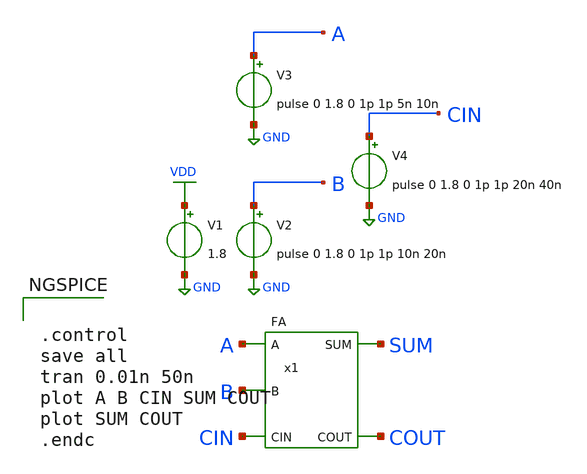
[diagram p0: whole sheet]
** sch_path: lib/xschem/test_FA.sch
**.subckt test_FA
V2 B GND pulse 0 1.8 0 1p 1p 10n 20n
V1 VDD GND 1.8
V3 A GND pulse 0 1.8 0 1p 1p 5n 10n
x1 SUM COUT A B CIN VDD GND FA
V4 CIN GND pulse 0 1.8 0 1p 1p 20n 40n
**** begin user architecture code

.lib $::SKYWATER_MODELS/sky130.lib.spice tt


**** end user architecture code
**.ends

* expanding   symbol:  FA.sym # of pins=5
** sym_path: lib/xschem/FA.sym
** sch_path: lib/xschem/FA.sch
.subckt FA SUM COUT A B CIN VCCPIN VSSPIN
*.opin COUT
*.ipin A
*.ipin B
*.ipin CIN
*.opin SUM
x1 net2 CIN net1 VCCPIN VSSPIN AND2X1
x2 net1 A B VCCPIN VSSPIN XOR2X1
x3 SUM net1 CIN VCCPIN VSSPIN XOR2X1
x4 net3 B A VCCPIN VSSPIN AND2X1
x5 COUT net2 net3 VCCPIN VSSPIN OR2X1
.ends


* expanding   symbol:  AND2X1.sym # of pins=3
** sym_path: lib/xschem/AND2X1.sym
** sch_path: lib/xschem/AND2X1.sch
.subckt AND2X1 Y A B VCCPIN VSSPIN
*.ipin A
*.ipin B
*.opin Y
x1 net1 A B NAND2X1
x2 Y net1 INVX1
.ends


* expanding   symbol:  XOR2X1.sym # of pins=3
** sym_path: lib/xschem/XOR2X1.sym
** sch_path: lib/xschem/XOR2X1.sch
.subckt XOR2X1 Y A B VCCPIN VSSPIN
*.ipin A
*.opin Y
*.ipin B
XM1 net6 A VSSPIN GND sky130_fd_pr__nfet_01v8 L=0.15 W=3 nf=1 ad='int((nf+1)/2) * W/nf * 0.29' as='int((nf+2)/2) * W/nf * 0.29'
+ pd='2*int((nf+1)/2) * (W/nf + 0.29)' ps='2*int((nf+2)/2) * (W/nf + 0.29)' nrd='0.29 / W' nrs='0.29 / W'
+ sa=0 sb=0 sd=0 mult=1 m=1
XM2 net6 A VCCPIN VDD sky130_fd_pr__pfet_01v8 L=0.15 W=2 nf=1 ad='int((nf+1)/2) * W/nf * 0.29' as='int((nf+2)/2) * W/nf * 0.29'
+ pd='2*int((nf+1)/2) * (W/nf + 0.29)' ps='2*int((nf+2)/2) * (W/nf + 0.29)' nrd='0.29 / W' nrs='0.29 / W'
+ sa=0 sb=0 sd=0 mult=1 m=1
XM3 net3 B VSSPIN GND sky130_fd_pr__nfet_01v8 L=0.15 W=3 nf=1 ad='int((nf+1)/2) * W/nf * 0.29' as='int((nf+2)/2) * W/nf * 0.29'
+ pd='2*int((nf+1)/2) * (W/nf + 0.29)' ps='2*int((nf+2)/2) * (W/nf + 0.29)' nrd='0.29 / W' nrs='0.29 / W'
+ sa=0 sb=0 sd=0 mult=1 m=1
XM4 net3 B VCCPIN VDD sky130_fd_pr__pfet_01v8 L=0.15 W=2 nf=1 ad='int((nf+1)/2) * W/nf * 0.29' as='int((nf+2)/2) * W/nf * 0.29'
+ pd='2*int((nf+1)/2) * (W/nf + 0.29)' ps='2*int((nf+2)/2) * (W/nf + 0.29)' nrd='0.29 / W' nrs='0.29 / W'
+ sa=0 sb=0 sd=0 mult=1 m=1
XM5 net4 net3 VCCPIN VDD sky130_fd_pr__pfet_01v8 L=0.15 W=2 nf=1 ad='int((nf+1)/2) * W/nf * 0.29' as='int((nf+2)/2) * W/nf * 0.29'
+ pd='2*int((nf+1)/2) * (W/nf + 0.29)' ps='2*int((nf+2)/2) * (W/nf + 0.29)' nrd='0.29 / W' nrs='0.29 / W'
+ sa=0 sb=0 sd=0 mult=1 m=1
XM6 Y A net4 VDD sky130_fd_pr__pfet_01v8 L=0.15 W=2 nf=1 ad='int((nf+1)/2) * W/nf * 0.29' as='int((nf+2)/2) * W/nf * 0.29'
+ pd='2*int((nf+1)/2) * (W/nf + 0.29)' ps='2*int((nf+2)/2) * (W/nf + 0.29)' nrd='0.29 / W' nrs='0.29 / W'
+ sa=0 sb=0 sd=0 mult=1 m=1
XM7 net2 B VCCPIN VDD sky130_fd_pr__pfet_01v8 L=0.15 W=2 nf=1 ad='int((nf+1)/2) * W/nf * 0.29' as='int((nf+2)/2) * W/nf * 0.29'
+ pd='2*int((nf+1)/2) * (W/nf + 0.29)' ps='2*int((nf+2)/2) * (W/nf + 0.29)' nrd='0.29 / W' nrs='0.29 / W'
+ sa=0 sb=0 sd=0 mult=1 m=1
XM8 Y net6 net2 VDD sky130_fd_pr__pfet_01v8 L=0.15 W=2 nf=1 ad='int((nf+1)/2) * W/nf * 0.29' as='int((nf+2)/2) * W/nf * 0.29'
+ pd='2*int((nf+1)/2) * (W/nf + 0.29)' ps='2*int((nf+2)/2) * (W/nf + 0.29)' nrd='0.29 / W' nrs='0.29 / W'
+ sa=0 sb=0 sd=0 mult=1 m=1
XM9 Y net6 net1 GND sky130_fd_pr__nfet_01v8 L=0.15 W=3 nf=1 ad='int((nf+1)/2) * W/nf * 0.29' as='int((nf+2)/2) * W/nf * 0.29'
+ pd='2*int((nf+1)/2) * (W/nf + 0.29)' ps='2*int((nf+2)/2) * (W/nf + 0.29)' nrd='0.29 / W' nrs='0.29 / W'
+ sa=0 sb=0 sd=0 mult=1 m=1
XM10 net1 net3 VSSPIN GND sky130_fd_pr__nfet_01v8 L=0.15 W=3 nf=1 ad='int((nf+1)/2) * W/nf * 0.29' as='int((nf+2)/2) * W/nf * 0.29'
+ pd='2*int((nf+1)/2) * (W/nf + 0.29)' ps='2*int((nf+2)/2) * (W/nf + 0.29)' nrd='0.29 / W' nrs='0.29 / W'
+ sa=0 sb=0 sd=0 mult=1 m=1
XM11 Y A net5 GND sky130_fd_pr__nfet_01v8 L=0.15 W=3 nf=1 ad='int((nf+1)/2) * W/nf * 0.29' as='int((nf+2)/2) * W/nf * 0.29'
+ pd='2*int((nf+1)/2) * (W/nf + 0.29)' ps='2*int((nf+2)/2) * (W/nf + 0.29)' nrd='0.29 / W' nrs='0.29 / W'
+ sa=0 sb=0 sd=0 mult=1 m=1
XM12 net5 B VSSPIN GND sky130_fd_pr__nfet_01v8 L=0.15 W=3 nf=1 ad='int((nf+1)/2) * W/nf * 0.29' as='int((nf+2)/2) * W/nf * 0.29'
+ pd='2*int((nf+1)/2) * (W/nf + 0.29)' ps='2*int((nf+2)/2) * (W/nf + 0.29)' nrd='0.29 / W' nrs='0.29 / W'
+ sa=0 sb=0 sd=0 mult=1 m=1
XM13 net4 net3 VCCPIN VDD sky130_fd_pr__pfet_01v8 L=0.15 W=2 nf=1 ad='int((nf+1)/2) * W/nf * 0.29' as='int((nf+2)/2) * W/nf * 0.29'
+ pd='2*int((nf+1)/2) * (W/nf + 0.29)' ps='2*int((nf+2)/2) * (W/nf + 0.29)' nrd='0.29 / W' nrs='0.29 / W'
+ sa=0 sb=0 sd=0 mult=1 m=1
XM14 Y A net4 VDD sky130_fd_pr__pfet_01v8 L=0.15 W=2 nf=1 ad='int((nf+1)/2) * W/nf * 0.29' as='int((nf+2)/2) * W/nf * 0.29'
+ pd='2*int((nf+1)/2) * (W/nf + 0.29)' ps='2*int((nf+2)/2) * (W/nf + 0.29)' nrd='0.29 / W' nrs='0.29 / W'
+ sa=0 sb=0 sd=0 mult=1 m=1
XM15 net2 B VCCPIN VDD sky130_fd_pr__pfet_01v8 L=0.15 W=2 nf=1 ad='int((nf+1)/2) * W/nf * 0.29' as='int((nf+2)/2) * W/nf * 0.29'
+ pd='2*int((nf+1)/2) * (W/nf + 0.29)' ps='2*int((nf+2)/2) * (W/nf + 0.29)' nrd='0.29 / W' nrs='0.29 / W'
+ sa=0 sb=0 sd=0 mult=1 m=1
XM16 Y net6 net2 VDD sky130_fd_pr__pfet_01v8 L=0.15 W=2 nf=1 ad='int((nf+1)/2) * W/nf * 0.29' as='int((nf+2)/2) * W/nf * 0.29'
+ pd='2*int((nf+1)/2) * (W/nf + 0.29)' ps='2*int((nf+2)/2) * (W/nf + 0.29)' nrd='0.29 / W' nrs='0.29 / W'
+ sa=0 sb=0 sd=0 mult=1 m=1
XM17 net3 B VCCPIN VDD sky130_fd_pr__pfet_01v8 L=0.15 W=2 nf=1 ad='int((nf+1)/2) * W/nf * 0.29' as='int((nf+2)/2) * W/nf * 0.29'
+ pd='2*int((nf+1)/2) * (W/nf + 0.29)' ps='2*int((nf+2)/2) * (W/nf + 0.29)' nrd='0.29 / W' nrs='0.29 / W'
+ sa=0 sb=0 sd=0 mult=1 m=1
XM18 net6 A VCCPIN VDD sky130_fd_pr__pfet_01v8 L=0.15 W=2 nf=1 ad='int((nf+1)/2) * W/nf * 0.29' as='int((nf+2)/2) * W/nf * 0.29'
+ pd='2*int((nf+1)/2) * (W/nf + 0.29)' ps='2*int((nf+2)/2) * (W/nf + 0.29)' nrd='0.29 / W' nrs='0.29 / W'
+ sa=0 sb=0 sd=0 mult=1 m=1
.ends


* expanding   symbol:  OR2X1.sym # of pins=3
** sym_path: lib/xschem/OR2X1.sym
** sch_path: lib/xschem/OR2X1.sch
.subckt OR2X1 Y A B VCCPIN VSSPIN
*.ipin A
*.ipin B
*.opin Y
x1 net1 A B NOR2X1
x2 Y net1 INVX1
.ends


* expanding   symbol:  NAND2X1.sym # of pins=3
** sym_path: lib/xschem/NAND2X1.sym
** sch_path: lib/xschem/NAND2X1.sch
.subckt NAND2X1 Y A B
*.ipin A
*.opin Y
*.ipin B
XM1 Y A VDD VDD sky130_fd_pr__pfet_01v8 L=0.15 W=2 nf=1 ad='int((nf+1)/2) * W/nf * 0.29' as='int((nf+2)/2) * W/nf * 0.29'
+ pd='2*int((nf+1)/2) * (W/nf + 0.29)' ps='2*int((nf+2)/2) * (W/nf + 0.29)' nrd='0.29 / W' nrs='0.29 / W'
+ sa=0 sb=0 sd=0 mult=1 m=1
XM5 Y A net1 VSS sky130_fd_pr__nfet_01v8 L=0.15 W=3 nf=1 ad='int((nf+1)/2) * W/nf * 0.29' as='int((nf+2)/2) * W/nf * 0.29'
+ pd='2*int((nf+1)/2) * (W/nf + 0.29)' ps='2*int((nf+2)/2) * (W/nf + 0.29)' nrd='0.29 / W' nrs='0.29 / W'
+ sa=0 sb=0 sd=0 mult=1 m=1
XM2 Y A VDD VDD sky130_fd_pr__pfet_01v8 L=0.15 W=2 nf=1 ad='int((nf+1)/2) * W/nf * 0.29' as='int((nf+2)/2) * W/nf * 0.29'
+ pd='2*int((nf+1)/2) * (W/nf + 0.29)' ps='2*int((nf+2)/2) * (W/nf + 0.29)' nrd='0.29 / W' nrs='0.29 / W'
+ sa=0 sb=0 sd=0 mult=1 m=1
XM3 Y B VDD VDD sky130_fd_pr__pfet_01v8 L=0.15 W=2 nf=1 ad='int((nf+1)/2) * W/nf * 0.29' as='int((nf+2)/2) * W/nf * 0.29'
+ pd='2*int((nf+1)/2) * (W/nf + 0.29)' ps='2*int((nf+2)/2) * (W/nf + 0.29)' nrd='0.29 / W' nrs='0.29 / W'
+ sa=0 sb=0 sd=0 mult=1 m=1
XM4 Y B VDD VDD sky130_fd_pr__pfet_01v8 L=0.15 W=2 nf=1 ad='int((nf+1)/2) * W/nf * 0.29' as='int((nf+2)/2) * W/nf * 0.29'
+ pd='2*int((nf+1)/2) * (W/nf + 0.29)' ps='2*int((nf+2)/2) * (W/nf + 0.29)' nrd='0.29 / W' nrs='0.29 / W'
+ sa=0 sb=0 sd=0 mult=1 m=1
XM6 net1 B VSS VSS sky130_fd_pr__nfet_01v8 L=0.15 W=3 nf=1 ad='int((nf+1)/2) * W/nf * 0.29' as='int((nf+2)/2) * W/nf * 0.29'
+ pd='2*int((nf+1)/2) * (W/nf + 0.29)' ps='2*int((nf+2)/2) * (W/nf + 0.29)' nrd='0.29 / W' nrs='0.29 / W'
+ sa=0 sb=0 sd=0 mult=1 m=1
.ends


* expanding   symbol:  NOR2X1.sym # of pins=3
** sym_path: lib/xschem/NOR2X1.sym
** sch_path: lib/xschem/NOR2X1.sch
.subckt NOR2X1 Y A B
*.opin Y
*.ipin A
*.ipin B
XM1 Y A VSS VSS sky130_fd_pr__nfet_01v8 L=0.15 W=3 nf=1 ad='int((nf+1)/2) * W/nf * 0.29' as='int((nf+2)/2) * W/nf * 0.29'
+ pd='2*int((nf+1)/2) * (W/nf + 0.29)' ps='2*int((nf+2)/2) * (W/nf + 0.29)' nrd='0.29 / W' nrs='0.29 / W'
+ sa=0 sb=0 sd=0 mult=1 m=1
XM2 net1 A VDD VDD sky130_fd_pr__pfet_01v8 L=0.15 W=2 nf=1 ad='int((nf+1)/2) * W/nf * 0.29' as='int((nf+2)/2) * W/nf * 0.29'
+ pd='2*int((nf+1)/2) * (W/nf + 0.29)' ps='2*int((nf+2)/2) * (W/nf + 0.29)' nrd='0.29 / W' nrs='0.29 / W'
+ sa=0 sb=0 sd=0 mult=2 m=2
XM3 Y B VSS VSS sky130_fd_pr__nfet_01v8 L=0.15 W=3 nf=1 ad='int((nf+1)/2) * W/nf * 0.29' as='int((nf+2)/2) * W/nf * 0.29'
+ pd='2*int((nf+1)/2) * (W/nf + 0.29)' ps='2*int((nf+2)/2) * (W/nf + 0.29)' nrd='0.29 / W' nrs='0.29 / W'
+ sa=0 sb=0 sd=0 mult=1 m=1
XM5 Y B net1 VDD sky130_fd_pr__pfet_01v8 L=0.15 W=2 nf=1 ad='int((nf+1)/2) * W/nf * 0.29' as='int((nf+2)/2) * W/nf * 0.29'
+ pd='2*int((nf+1)/2) * (W/nf + 0.29)' ps='2*int((nf+2)/2) * (W/nf + 0.29)' nrd='0.29 / W' nrs='0.29 / W'
+ sa=0 sb=0 sd=0 mult=2 m=2
.ends

.GLOBAL VDD
.GLOBAL GND
**** begin user architecture code


.control
save all
tran 0.01n 50n
plot A B CIN SUM COUT
plot SUM COUT
.endc


**** end user architecture code
.end
